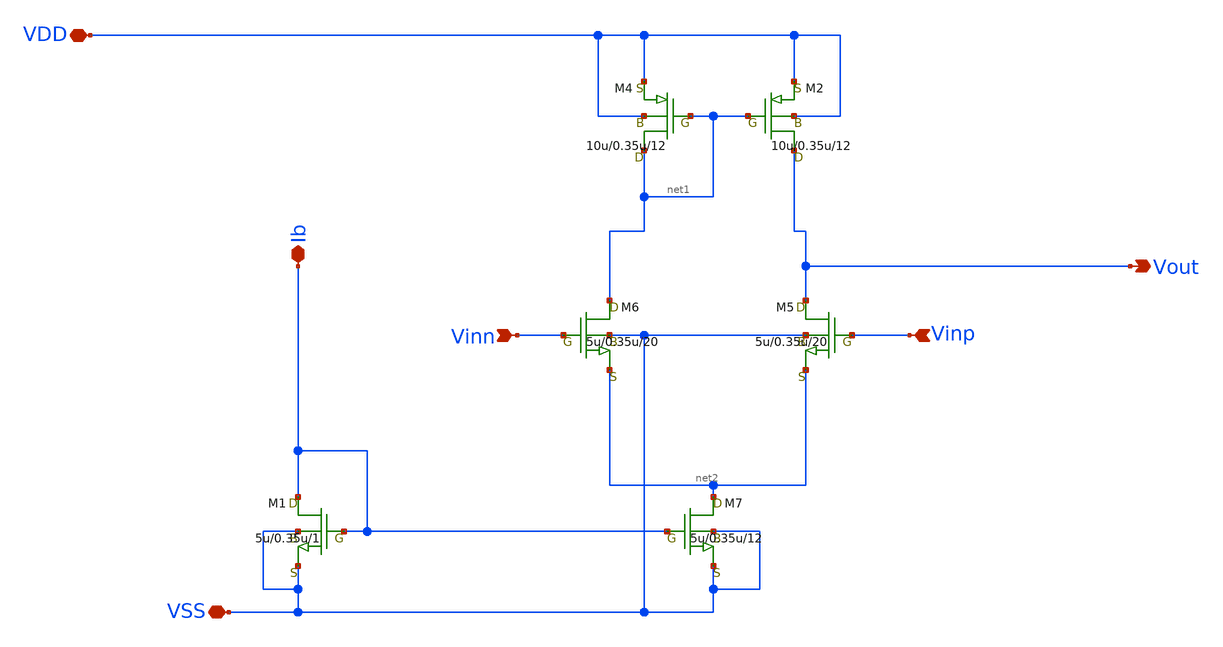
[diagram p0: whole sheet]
** sch_path: OPAmpNforRTR.sch
**.subckt OPAmpNforRTR Vout Vinn Vinp Ib VDD VSS
*.opin Vout
*.ipin Vinn
*.ipin Vinp
*.iopin Ib
*.iopin VDD
*.iopin VSS
M5 Vout Vinp net2 VSS nch w=5u l=0.35u as=0 ps=0 ad=0 pd=0 m=20
M6 net1 Vinn net2 VSS nch w=5u l=0.35u as=0 ps=0 ad=0 pd=0 m=20
M2 Vout net1 VDD VDD pch w=10u l=0.35u as=0 ps=0 ad=0 pd=0 m=12
M4 net1 net1 VDD VDD pch w=10u l=0.35u as=0 ps=0 ad=0 pd=0 m=12
M7 net2 Ib VSS VSS nch w=5u l=0.35u as=0 ps=0 ad=0 pd=0 m=12
M1 Ib Ib VSS VSS nch w=5u l=0.35u as=0 ps=0 ad=0 pd=0 m=1
**.ends
.end
